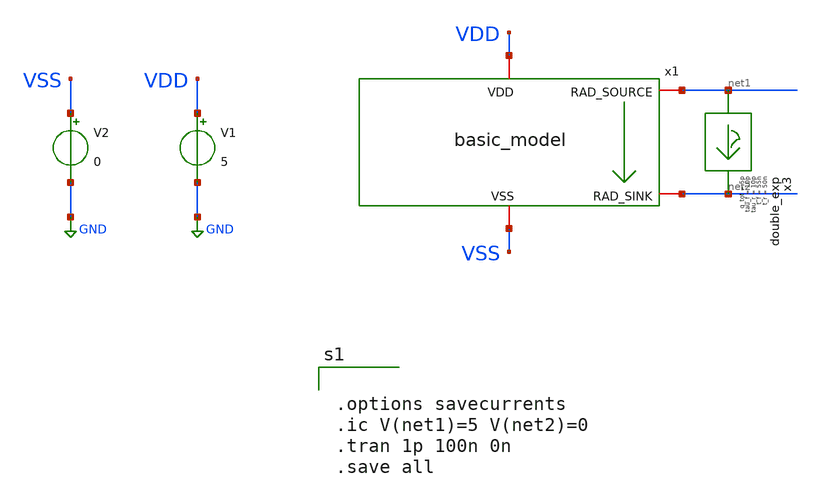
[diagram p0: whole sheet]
** sch_path: basic_test.sch
**.subckt basic_test
V1 VDD GND 5
V2 VSS GND 0
x3 net1 net2 double_exp t_r=50n tau_r=10p t_f=55n tau_f=10p q_tot=5p
x1 VDD net1 net2 VSS basic_model IS_N=1e-16 BF_N=100 VAF_N=50 IKF_N=0.01 CJE_N=0.2p CJC_N=0.1p
+ TF_N=0.2n TR_N=2n IS_P=1e-16 BF_P=100 VAF_P=50 IKF_P=0.01 CJE_P=0.3p CJC_P=0.15p TF_P=0.3n TR_P=3n
**** begin user architecture code


.options savecurrents
.ic V(net1)=5 V(net2)=0
.tran 1p 100n 0n
.save all




.include /usr/local/share/rad_modeling_blocks/rad_modeling_blocks.spice


**** end user architecture code
**.ends

* expanding   symbol:  double_exp.sym # of pins=2
** sym_path: xschem_rad_library/double_exp.sym
** sch_path: xschem_rad_library/double_exp.sch
.subckt double_exp in out  t_r=0 t_f=0 tau_r=0 tau_f=0 q_tot=0
*.opin OUT
*.ipin IN
I1 IN OUT EXP(0 {q_tot / (t_f-t_r+tau_f-tau_r)} {t_r} {tau_r} {t_f} {tau_f})
.ends


* expanding   symbol:  OSCRE/latchup/basic_model.sym # of pins=4
** sym_path: latchup/basic_model.sym
** sch_path: latchup/basic_model.sch
.subckt basic_model VDD RAD_SOURCE RAD_SINK VSS   IS_N=1e-16  BF_N=100  VAF_N=100  IKF_N=0.1
+  CJE_N=2p  CJC_N=2p  TF_N=0.1n  TR_N=10n  IS_P=1e-16  BF_P=100  VAF_P=100  IKF_P=0.1  CJE_P=2p  CJC_P=2p
+  TF_P=0.1n  TR_P=10n
*.iopin VDD
*.iopin VSS
*.iopin RAD_SOURCE
*.iopin RAD_SINK
Q1 RAD_SINK RAD_SOURCE VDD pnp_cust area=1 m=1
Q2 RAD_SOURCE RAD_SINK VSS npn_cust area=1 m=1
R3 RAD_SINK VSS 1000 m=1
R4 VDD RAD_SOURCE 1000 m=1
**** begin user architecture code


.model npn_cust npn (IS={IS_N} BF={BF_N} VAF={VAF_N} IKF={IKF_N} CJE={CJE_N} CJC={CJC_N} TF={TF_N} TR={TR_N})
.model pnp_cust pnp (IS={IS_P} BF={BF_P} VAF={VAF_P} IKF={IKF_P} CJE={CJE_P} CJC={CJC_N} TF={TF_N} TR={TR_P})


**** end user architecture code
.ends

.GLOBAL GND
.end
